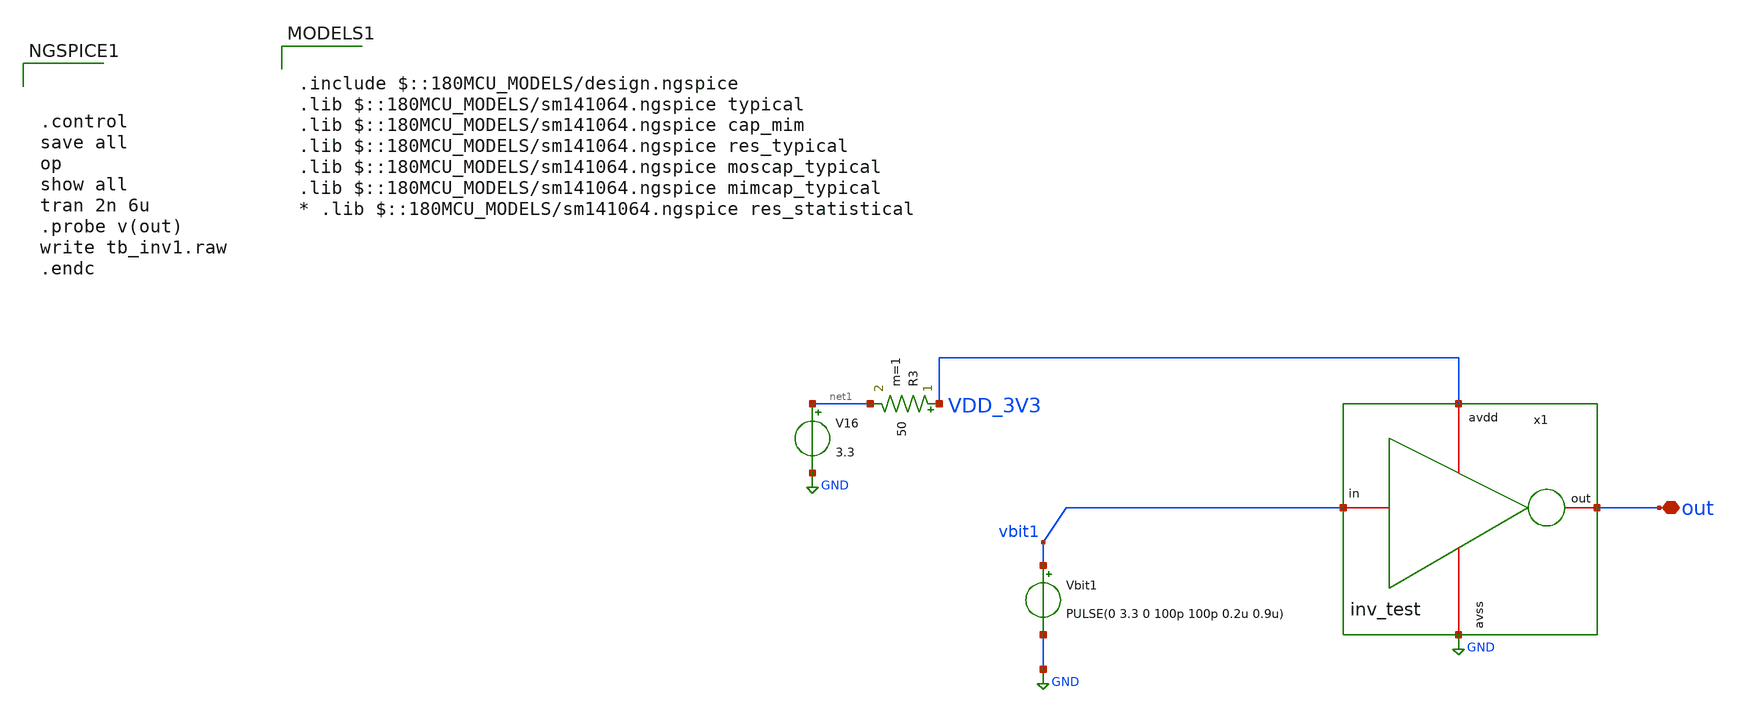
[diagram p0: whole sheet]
** sch_path: designs/libs/untitled.sch
**.subckt untitled out
*.iopin out
x1 VDD_3V3 vbit1 out GND inv_test
Vbit1 vbit1 GND PULSE(0 3.3 0 100p 100p 0.2u 0.9u)
V16 net1 GND 3.3
R3 VDD_3V3 net1 50 m=1
**** begin user architecture code



.control
save all
op
show all
tran 2n 6u
.probe v(out)
write tb_inv1.raw
.endc



.include $::180MCU_MODELS/design.ngspice
.lib $::180MCU_MODELS/sm141064.ngspice typical
.lib $::180MCU_MODELS/sm141064.ngspice cap_mim
.lib $::180MCU_MODELS/sm141064.ngspice res_typical
.lib $::180MCU_MODELS/sm141064.ngspice moscap_typical
.lib $::180MCU_MODELS/sm141064.ngspice mimcap_typical
* .lib $::180MCU_MODELS/sm141064.ngspice res_statistical

**** end user architecture code
**.ends

* expanding   symbol:  libs/WK_Kadam/inv_test.sym # of pins=4
** sym_path: libs/WK_Kadam/inv_test.sym
** sch_path: libs/WK_Kadam/inv_test.sch
.subckt inv_test avdd in out avss
*.iopin avdd
*.iopin avss
*.iopin in
*.iopin out
XM3 out in avss avss nfet_03v3 L=0.28u W=1u nf=1 ad='int((nf+1)/2) * W/nf * 0.18u' as='int((nf+2)/2) * W/nf * 0.18u'
+ pd='2*int((nf+1)/2) * (W/nf + 0.18u)' ps='2*int((nf+2)/2) * (W/nf + 0.18u)' nrd='0.18u / W' nrs='0.18u / W'
+ sa=0 sb=0 sd=0 m=1
XM4 out in avdd avdd pfet_03v3 L=0.28u W=2.5u nf=1 ad='int((nf+1)/2) * W/nf * 0.18u' as='int((nf+2)/2) * W/nf * 0.18u'
+ pd='2*int((nf+1)/2) * (W/nf + 0.18u)' ps='2*int((nf+2)/2) * (W/nf + 0.18u)' nrd='0.18u / W' nrs='0.18u / W'
+ sa=0 sb=0 sd=0 m=1
.ends

.GLOBAL GND
.end
